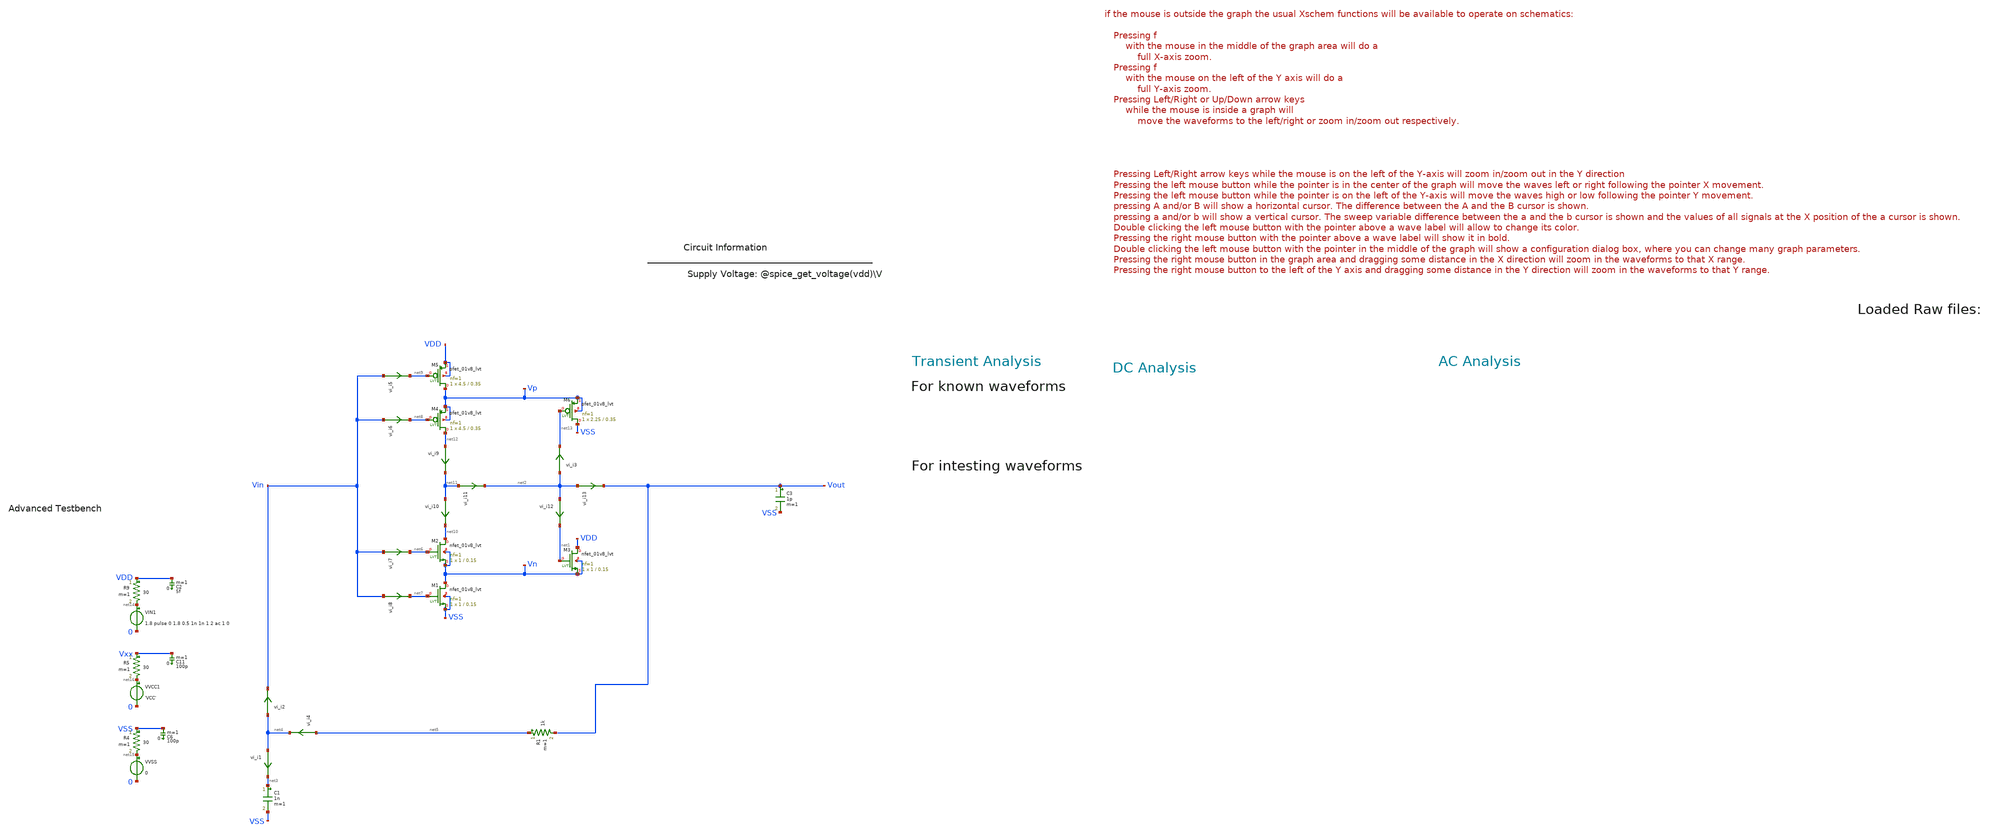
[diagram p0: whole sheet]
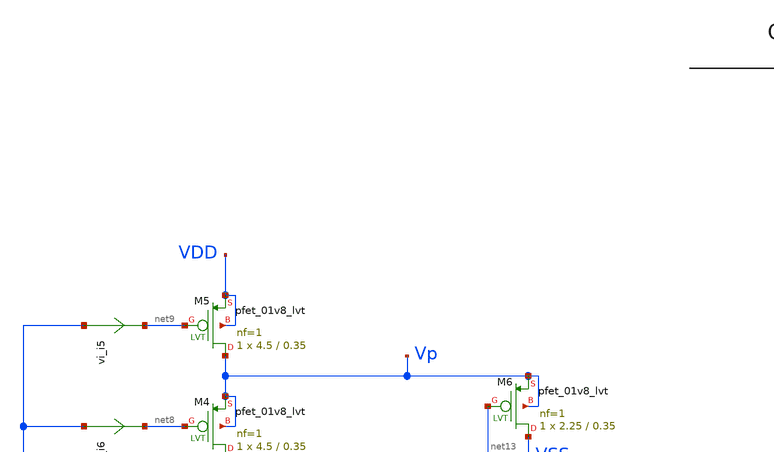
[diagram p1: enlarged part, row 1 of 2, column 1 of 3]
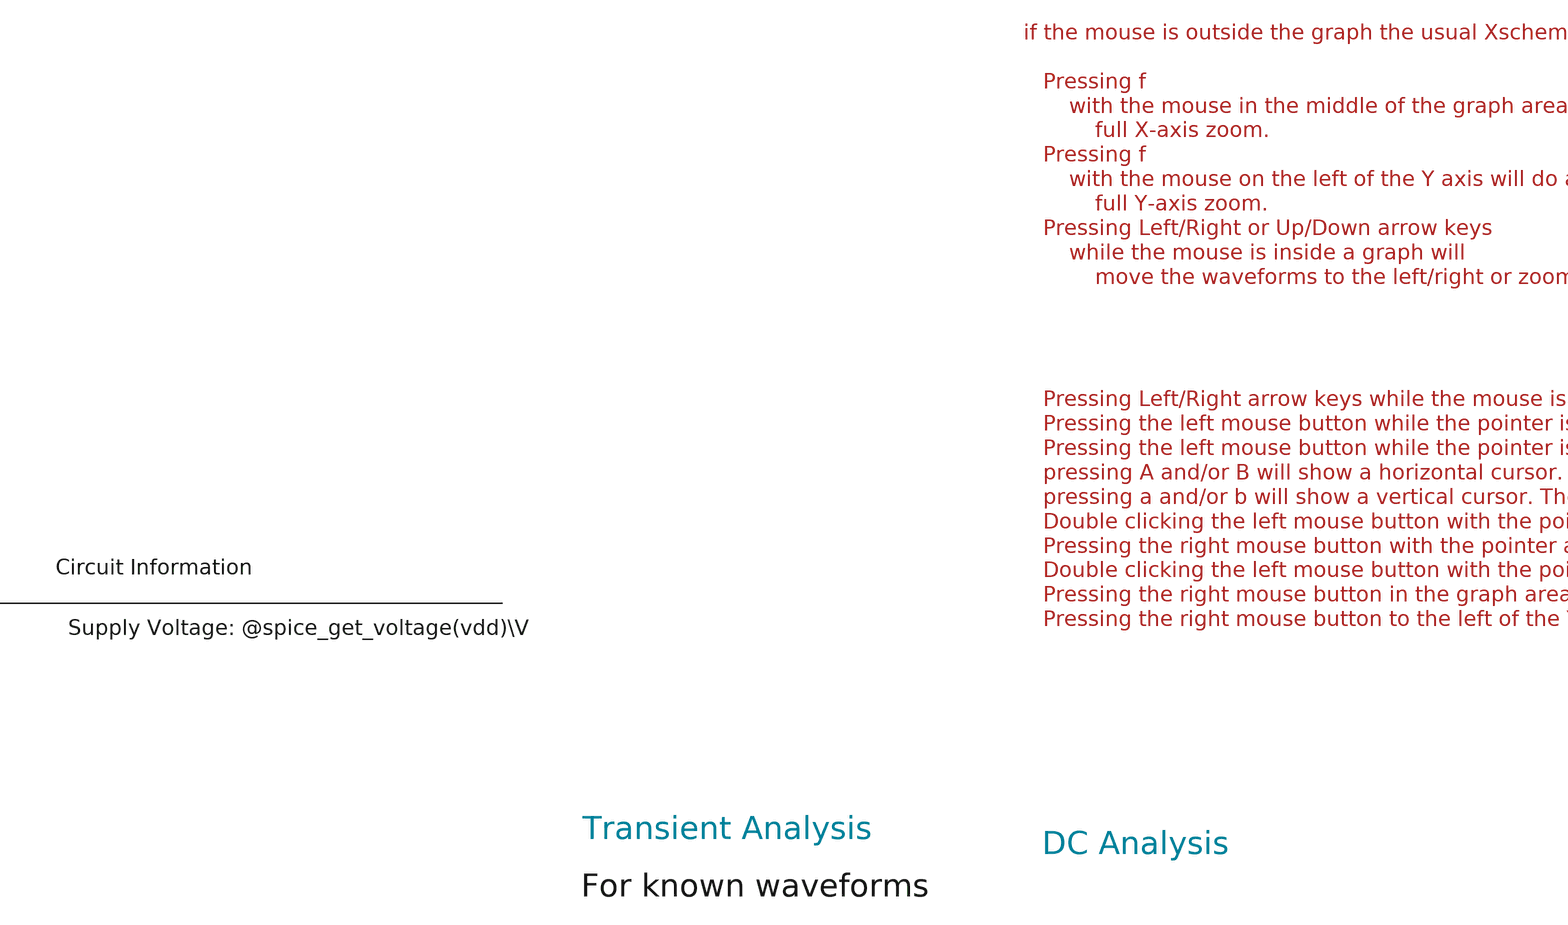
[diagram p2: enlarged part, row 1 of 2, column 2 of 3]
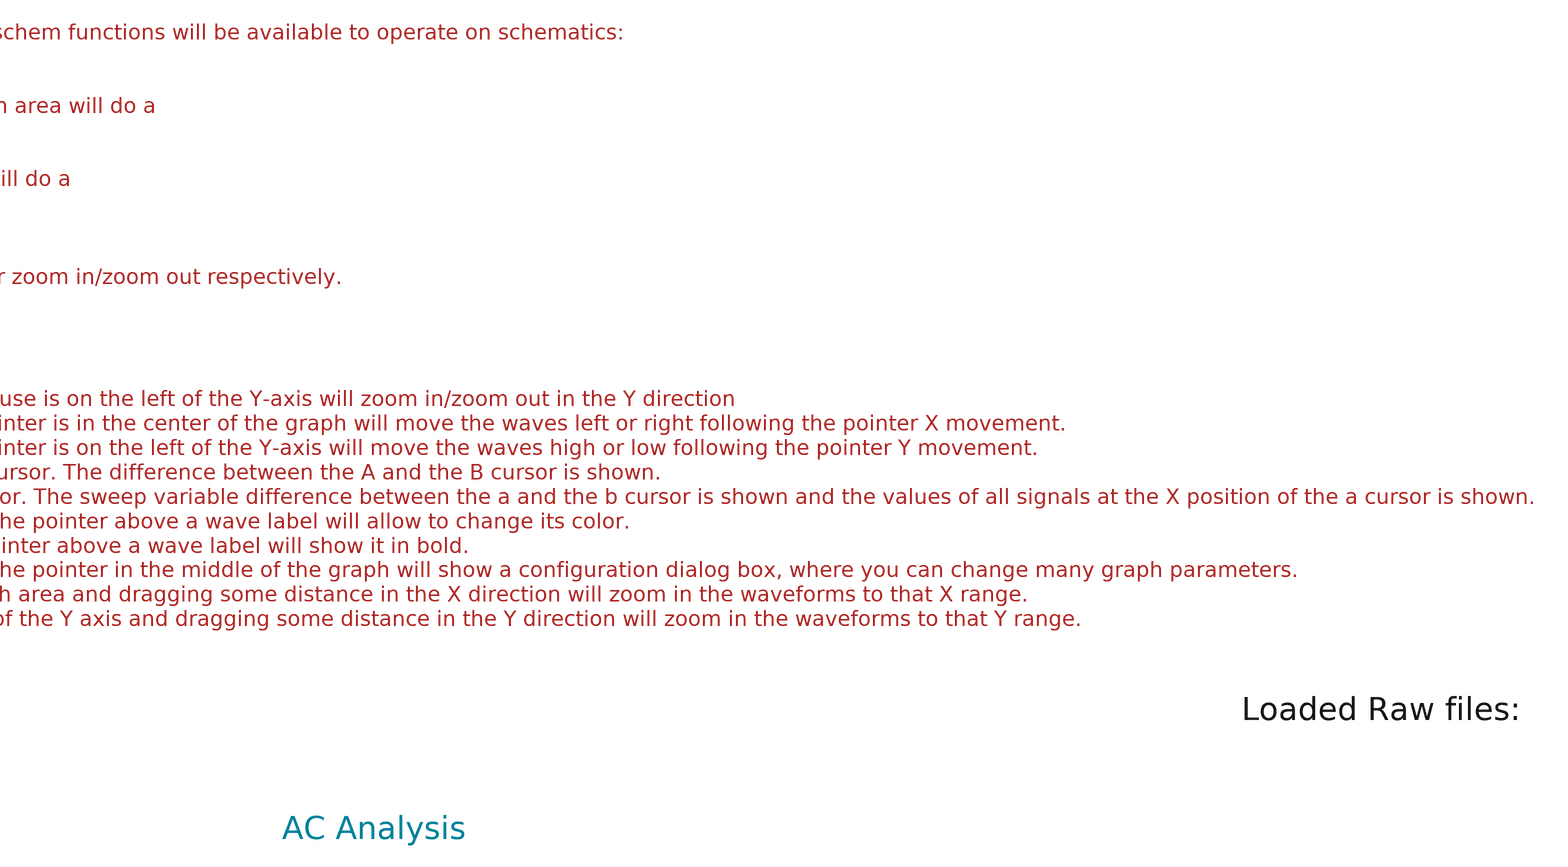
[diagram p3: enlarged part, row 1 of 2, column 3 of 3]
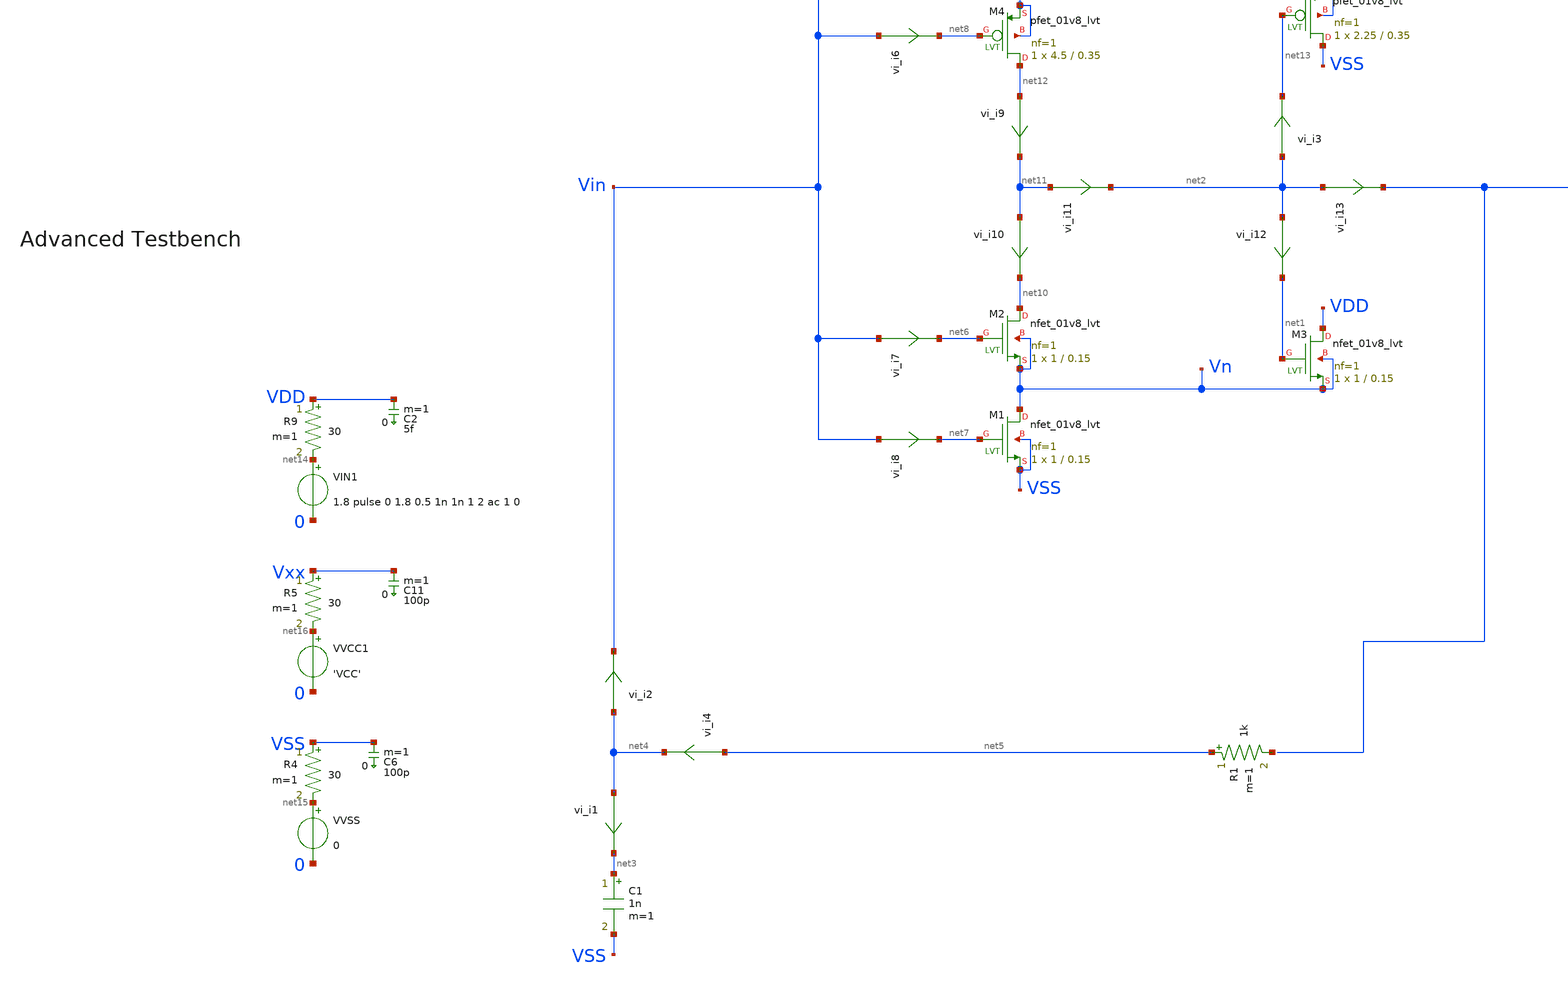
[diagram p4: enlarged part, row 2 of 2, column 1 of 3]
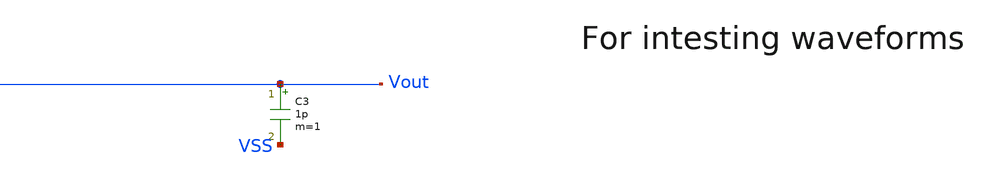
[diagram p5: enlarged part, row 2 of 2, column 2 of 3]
** sch_path: tt10-hdl/tt_um_test_commit/xschem/T1/schmTrigg/schmTrigg_anal_tb.sch
* Copyright (C) 1998-2024 Stefan Frederik Schippers
* This program is free software; you can redistribute it and/or modify
* it under the terms of the GNU General Public License as published by
* the Free Software Foundation; either version 2 of the License, or
* (at your option) any later version.
* This program is distributed in the hope that it will be useful,
* but WITHOUT ANY WARRANTY; without even the implied warranty of
* MERCHANTABILITY or FITNESS FOR A PARTICULAR PURPOSE.  See the
* GNU General Public License for more details.
* You should have received a copy of the GNU General Public License
* along with this program; if not, write to the Free Software
**.subckt schmTrigg_anal_tb
VIN1 net14 0 1.8 pulse 0 1.8 0.5 1n 1n 1 2 ac 1 0
VVSS net15 0 0
R4 VSS net15 30 m=1
C6 VSS 0 100p m=1
VVCC1 net16 0 'VCC'
R5 Vxx net16 30 m=1
C11 Vxx 0 100p m=1
R9 VDD net14 30 m=1
C2 VDD 0 5f m=1
XM5 Vp net9 VDD VDD sky130_fd_pr__pfet_01v8_lvt L=0.35 W=4.5 nf=1 ad='int((1 + 1)/2) * 4.5 / 1 * 0.29'
+ as='int((1 + 2)/2) * 4.5 / 1 * 0.29' pd='2*int((1 + 1)/2) * (4.5 / 1 + 0.29)' ps='2*int((1 + 2)/2) * (4.5 / 1 + 0.29)'
+ nrd='0.29 / 4.5 ' nrs='0.29 / 4.5 ' sa=0 sb=0 sd=0 mult=1 m=1
XM4 net12 net8 Vp Vp sky130_fd_pr__pfet_01v8_lvt L=0.35 W=4.5 nf=1 ad='int((1 + 1)/2) * 4.5 / 1 * 0.29'
+ as='int((1 + 2)/2) * 4.5 / 1 * 0.29' pd='2*int((1 + 1)/2) * (4.5 / 1 + 0.29)' ps='2*int((1 + 2)/2) * (4.5 / 1 + 0.29)'
+ nrd='0.29 / 4.5 ' nrs='0.29 / 4.5 ' sa=0 sb=0 sd=0 mult=1 m=1
XM6 VSS net13 Vp Vp sky130_fd_pr__pfet_01v8_lvt L=0.35 W=2.25 nf=1 ad='int((1 + 1)/2) * 2.25 / 1 * 0.29'
+ as='int((1 + 2)/2) * 2.25 / 1 * 0.29' pd='2*int((1 + 1)/2) * (2.25 / 1 + 0.29)' ps='2*int((1 + 2)/2) * (2.25 / 1 + 0.29)'
+ nrd='0.29 / 2.25 ' nrs='0.29 / 2.25 ' sa=0 sb=0 sd=0 mult=1 m=1
XM2 net10 net6 Vn Vn sky130_fd_pr__nfet_01v8_lvt L=0.15 W=1 nf=1 ad='int((1 + 1)/2) * 1 / 1 * 0.29' as='int((1 + 2)/2) * 1 / 1 * 0.29'
+ pd='2*int((1 + 1)/2) * (1 / 1 + 0.29)' ps='2*int((1 + 2)/2) * (1 / 1 + 0.29)' nrd='0.29 / 1 ' nrs='0.29 / 1 '
+ sa=0 sb=0 sd=0 mult=1 m=1
XM1 Vn net7 VSS VSS sky130_fd_pr__nfet_01v8_lvt L=0.15 W=1 nf=1 ad='int((1 + 1)/2) * 1 / 1 * 0.29' as='int((1 + 2)/2) * 1 / 1 * 0.29'
+ pd='2*int((1 + 1)/2) * (1 / 1 + 0.29)' ps='2*int((1 + 2)/2) * (1 / 1 + 0.29)' nrd='0.29 / 1 ' nrs='0.29 / 1 '
+ sa=0 sb=0 sd=0 mult=1 m=1
XM3 VDD net1 Vn Vn sky130_fd_pr__nfet_01v8_lvt L=0.15 W=1 nf=1 ad='int((1 + 1)/2) * 1 / 1 * 0.29' as='int((1 + 2)/2) * 1 / 1 * 0.29'
+ pd='2*int((1 + 1)/2) * (1 / 1 + 0.29)' ps='2*int((1 + 2)/2) * (1 / 1 + 0.29)' nrd='0.29 / 1 ' nrs='0.29 / 1 '
+ sa=0 sb=0 sd=0 mult=1 m=1
C1 net3 VSS 1n m=1
R1 net5 net17 1k m=1
vi_i1 net4 net3 0
.save i(vi_i1)
vi_i2 net4 Vin 0
.save i(vi_i2)
vi_i4 net5 net4 0
.save i(vi_i4)
vi_i5 Vin net9 0
.save i(vi_i5)
vi_i6 Vin net8 0
.save i(vi_i6)
vi_i7 Vin net6 0
.save i(vi_i7)
vi_i8 Vin net7 0
.save i(vi_i8)
vi_i9 net12 net11 0
.save i(vi_i9)
vi_i10 net11 net10 0
.save i(vi_i10)
vi_i11 net11 net2 0
.save i(vi_i11)
vi_i3 net2 net13 0
.save i(vi_i3)
vi_i12 net2 net1 0
.save i(vi_i12)
vi_i13 net2 Vout 0
.save i(vi_i13)
C3 Vout VSS 1p m=1
**** begin user architecture code



.temp 30
*.param IB=1n
.param VCC = 1.8

.option savecurrents
.save all @m1[gm]
.control
  save all alli
  op
  let power=-v(vcc) * i(vvcc)
  settype power power
  write template_adv_tb.raw
  set appendwrite

  *dc vin1 0 1.8 0.001
  *write template_adv_tb.raw

  tran 1m 3
  *tran 0.01n 15n
  write template_adv_tb.raw

  *ac dec 10 1 1G
  *remzerovec
  *write template_adv_tb.raw



  quit 0




.endc





** opencircuitdesign pdks install
.lib $::SKYWATER_MODELS/sky130.lib.spice tt
.include $::SKYWATER_STDCELLS/sky130_fd_sc_hd.spice


**** end user architecture code
**.ends
.end
